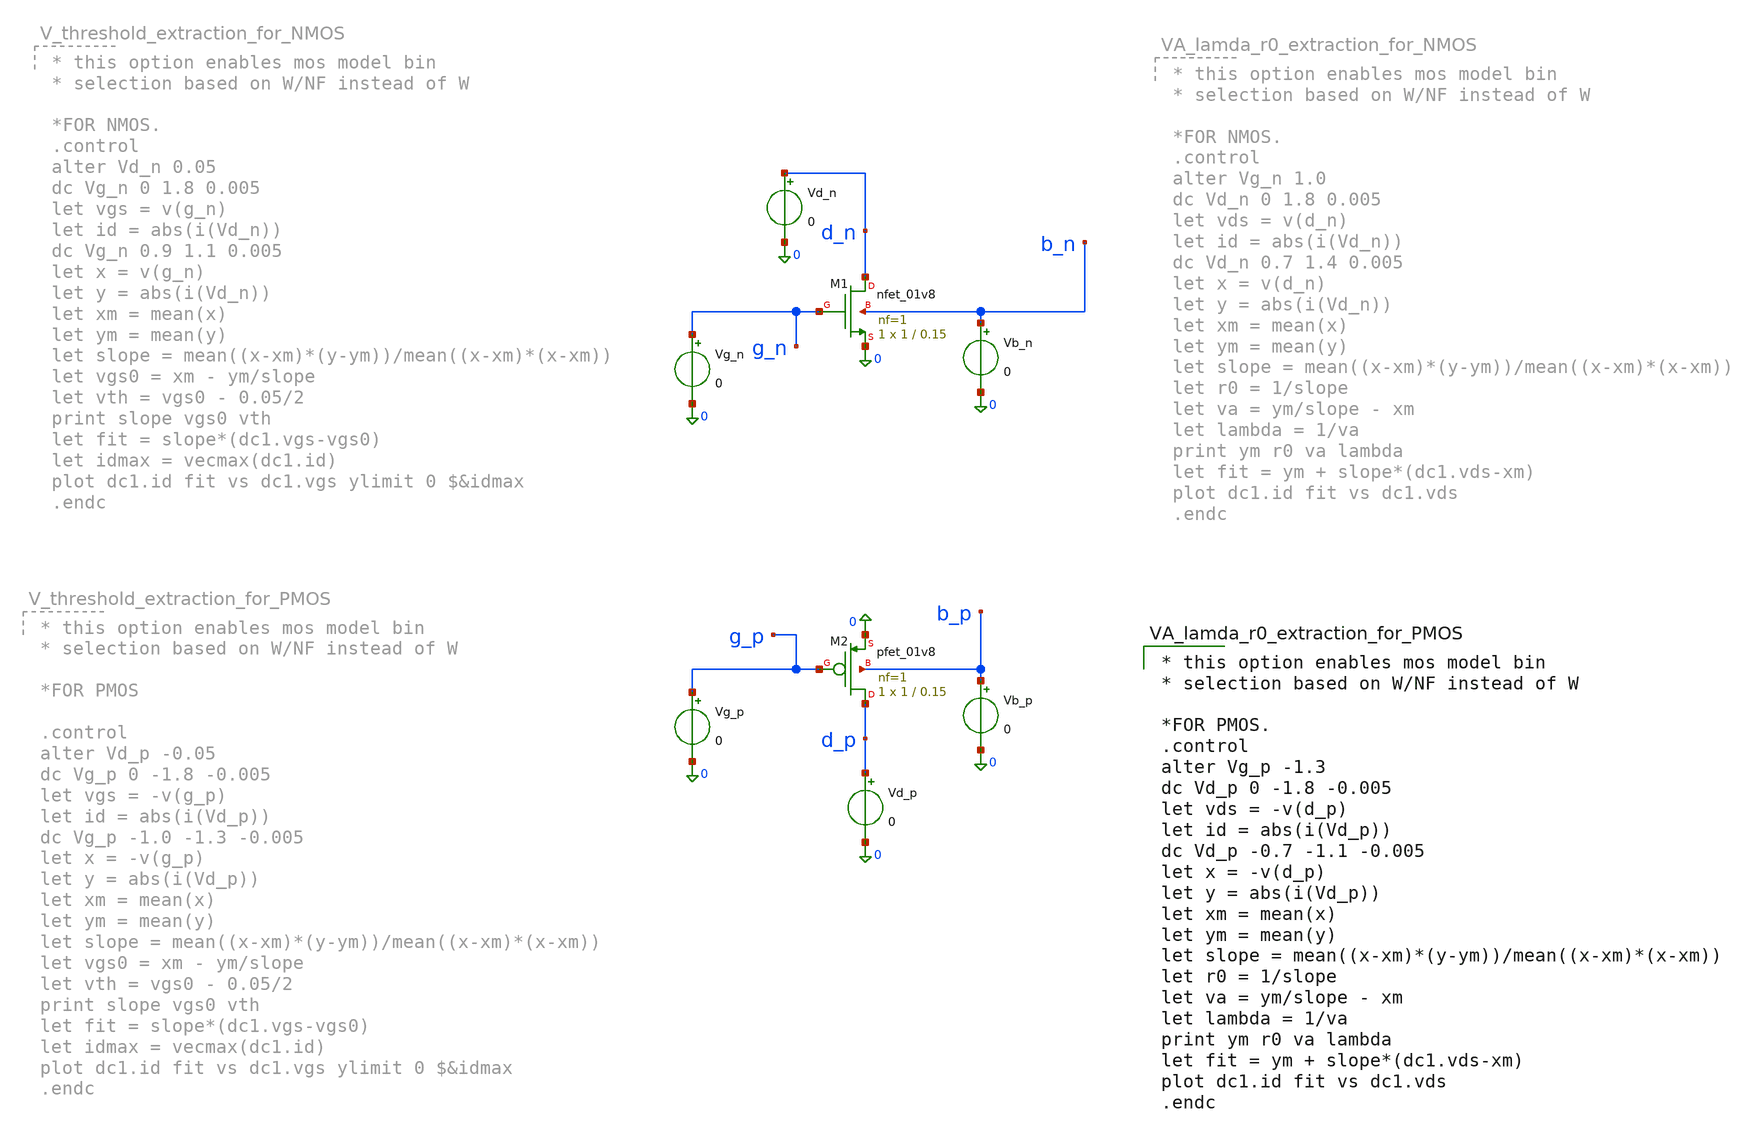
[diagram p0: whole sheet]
** sch_path: testcircuit/mos_parameter_extraction.sch
**.subckt mos_parameter_extraction
XM1 d_n g_n 0 b_n sky130_fd_pr__nfet_01v8 L=0.15 W=1 nf=1 ad='int((1 + 1)/2) * 1 / 1 * 0.29' as='int((1 + 2)/2) * 1 / 1 * 0.29'
+ pd='2*int((1 + 1)/2) * (1 / 1 + 0.29)' ps='2*int((1 + 2)/2) * (1 / 1 + 0.29)' nrd='0.29 / 1 ' nrs='0.29 / 1 '
+ sa=0 sb=0 sd=0 mult=1 m=1
XM2 d_p g_p 0 b_p sky130_fd_pr__pfet_01v8 L=0.15 W=1 nf=1 ad='int((1 + 1)/2) * 1 / 1 * 0.29' as='int((1 + 2)/2) * 1 / 1 * 0.29'
+ pd='2*int((1 + 1)/2) * (1 / 1 + 0.29)' ps='2*int((1 + 2)/2) * (1 / 1 + 0.29)' nrd='0.29 / 1 ' nrs='0.29 / 1 '
+ sa=0 sb=0 sd=0 mult=1 m=1
Vg_n g_n 0 0
Vd_n d_n 0 0
Vb_n b_n 0 0
Vg_p g_p 0 0
Vd_p d_p 0 0
Vb_p b_p 0 0
**** begin user architecture code

** opencircuitdesign pdks install
.lib $::SKYWATER_MODELS/sky130.lib.spice tt


* this option enables mos model bin
* selection based on W/NF instead of W

*FOR PMOS.
.control
alter Vg_p -1.3
dc Vd_p 0 -1.8 -0.005
let vds = -v(d_p)
let id = abs(i(Vd_p))
dc Vd_p -0.7 -1.1 -0.005
let x = -v(d_p)
let y = abs(i(Vd_p))
let xm = mean(x)
let ym = mean(y)
let slope = mean((x-xm)*(y-ym))/mean((x-xm)*(x-xm))
let r0 = 1/slope
let va = ym/slope - xm
let lambda = 1/va
print ym r0 va lambda
let fit = ym + slope*(dc1.vds-xm)
plot dc1.id fit vs dc1.vds
.endc


**** end user architecture code
**.ends
.end
